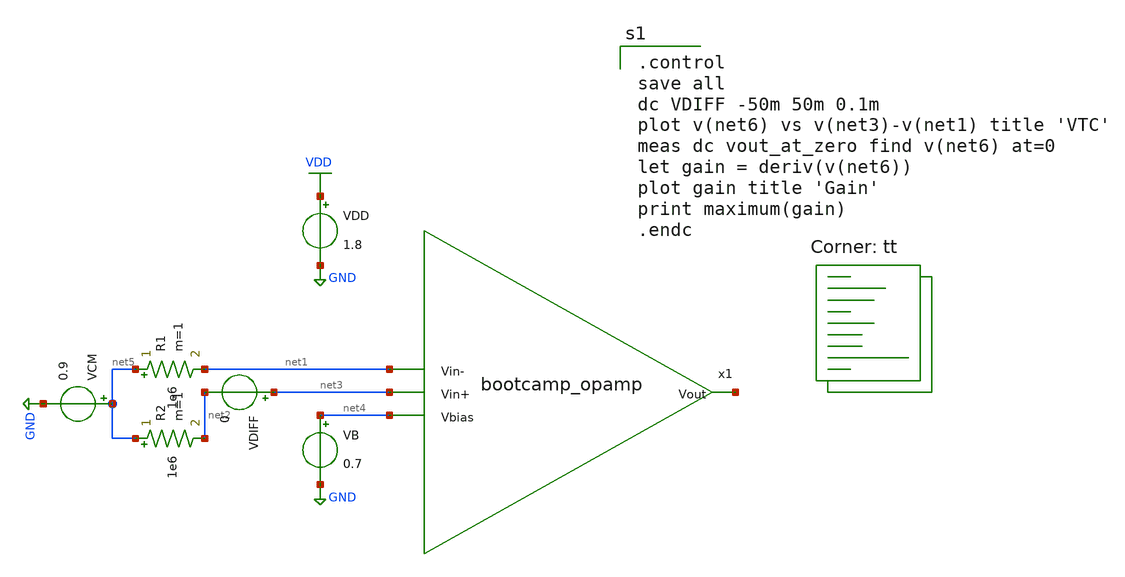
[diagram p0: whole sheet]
** sch_path: analog/schematics/tb_dc_analysis.sch
**.subckt tb_dc_analysis
x1 net6 net1 net3 net4 bootcamp_opamp
VDD VDD GND 1.8
VCM net5 GND 0.9
VB net4 GND 0.7
VDIFF net3 net2 0
R1 net5 net1 1e6 m=1
R2 net5 net2 1e6 m=1
**** begin user architecture code

.control
save all
dc VDIFF -50m 50m 0.1m
plot v(net6) vs v(net3)-v(net1) title 'VTC'
meas dc vout_at_zero find v(net6) at=0
let gain = deriv(v(net6))
plot gain title 'Gain'
print maximum(gain)
.endc

.lib $::SKYWATER_MODELS/sky130.lib.spice tt
**** end user architecture code
**.ends
.GLOBAL GND
.GLOBAL VDD
.end
